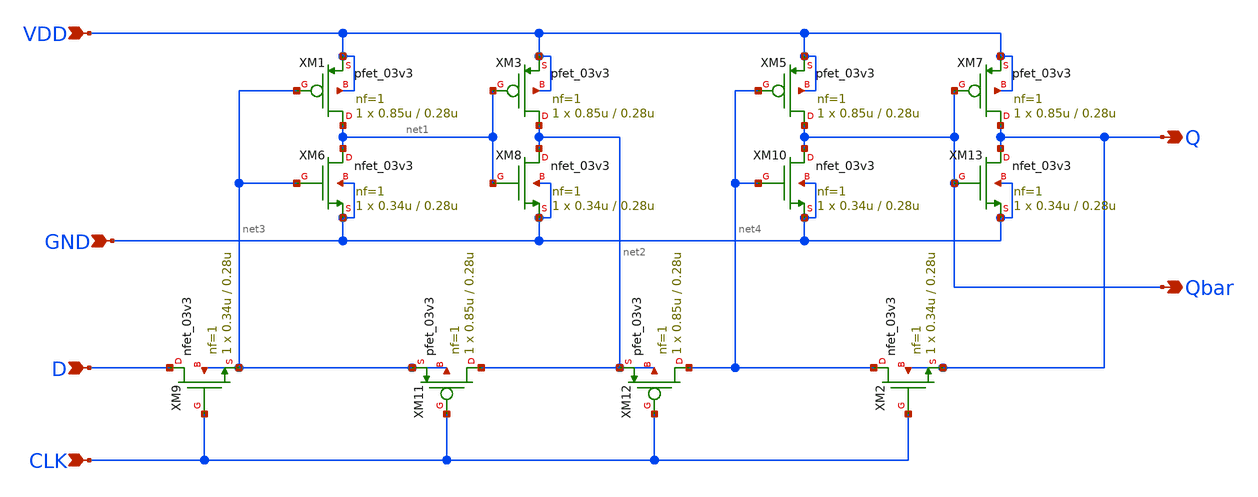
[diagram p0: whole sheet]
** sch_path: Project/1-on-chip/schematic/PNgen/dff.sch
**.subckt dff VDD Q GND D CLK Qbar
*.ipin VDD
*.opin Q
*.ipin GND
*.ipin D
*.ipin CLK
*.opin Qbar
XM9 D CLK net3 net3 nfet_03v3 L=0.28u W=0.34u nf=1 ad='int((nf+1)/2) * W/nf * 0.18u' as='int((nf+2)/2) * W/nf * 0.18u'
+ pd='2*int((nf+1)/2) * (W/nf + 0.18u)' ps='2*int((nf+2)/2) * (W/nf + 0.18u)' nrd='0.18u / W' nrs='0.18u / W'
+ sa=0 sb=0 sd=0 m=1
XM2 net4 CLK Q Q nfet_03v3 L=0.28u W=0.34u nf=1 ad='int((nf+1)/2) * W/nf * 0.18u' as='int((nf+2)/2) * W/nf * 0.18u'
+ pd='2*int((nf+1)/2) * (W/nf + 0.18u)' ps='2*int((nf+2)/2) * (W/nf + 0.18u)' nrd='0.18u / W' nrs='0.18u / W'
+ sa=0 sb=0 sd=0 m=1
XM6 net1 net3 GND GND nfet_03v3 L=0.28u W=0.34u nf=1 ad='int((nf+1)/2) * W/nf * 0.18u' as='int((nf+2)/2) * W/nf * 0.18u'
+ pd='2*int((nf+1)/2) * (W/nf + 0.18u)' ps='2*int((nf+2)/2) * (W/nf + 0.18u)' nrd='0.18u / W' nrs='0.18u / W'
+ sa=0 sb=0 sd=0 m=1
XM8 net2 net1 GND GND nfet_03v3 L=0.28u W=0.34u nf=1 ad='int((nf+1)/2) * W/nf * 0.18u' as='int((nf+2)/2) * W/nf * 0.18u'
+ pd='2*int((nf+1)/2) * (W/nf + 0.18u)' ps='2*int((nf+2)/2) * (W/nf + 0.18u)' nrd='0.18u / W' nrs='0.18u / W'
+ sa=0 sb=0 sd=0 m=1
XM10 Qbar net4 GND GND nfet_03v3 L=0.28u W=0.34u nf=1 ad='int((nf+1)/2) * W/nf * 0.18u' as='int((nf+2)/2) * W/nf * 0.18u'
+ pd='2*int((nf+1)/2) * (W/nf + 0.18u)' ps='2*int((nf+2)/2) * (W/nf + 0.18u)' nrd='0.18u / W' nrs='0.18u / W'
+ sa=0 sb=0 sd=0 m=1
XM13 Q Qbar GND GND nfet_03v3 L=0.28u W=0.34u nf=1 ad='int((nf+1)/2) * W/nf * 0.18u' as='int((nf+2)/2) * W/nf * 0.18u'
+ pd='2*int((nf+1)/2) * (W/nf + 0.18u)' ps='2*int((nf+2)/2) * (W/nf + 0.18u)' nrd='0.18u / W' nrs='0.18u / W'
+ sa=0 sb=0 sd=0 m=1
XM1 net1 net3 VDD VDD pfet_03v3 L=0.28u W=0.85u nf=1 ad='int((nf+1)/2) * W/nf * 0.18u' as='int((nf+2)/2) * W/nf * 0.18u'
+ pd='2*int((nf+1)/2) * (W/nf + 0.18u)' ps='2*int((nf+2)/2) * (W/nf + 0.18u)' nrd='0.18u / W' nrs='0.18u / W'
+ sa=0 sb=0 sd=0 m=1
XM3 net2 net1 VDD VDD pfet_03v3 L=0.28u W=0.85u nf=1 ad='int((nf+1)/2) * W/nf * 0.18u' as='int((nf+2)/2) * W/nf * 0.18u'
+ pd='2*int((nf+1)/2) * (W/nf + 0.18u)' ps='2*int((nf+2)/2) * (W/nf + 0.18u)' nrd='0.18u / W' nrs='0.18u / W'
+ sa=0 sb=0 sd=0 m=1
XM5 Qbar net4 VDD VDD pfet_03v3 L=0.28u W=0.85u nf=1 ad='int((nf+1)/2) * W/nf * 0.18u' as='int((nf+2)/2) * W/nf * 0.18u'
+ pd='2*int((nf+1)/2) * (W/nf + 0.18u)' ps='2*int((nf+2)/2) * (W/nf + 0.18u)' nrd='0.18u / W' nrs='0.18u / W'
+ sa=0 sb=0 sd=0 m=1
XM7 Q Qbar VDD VDD pfet_03v3 L=0.28u W=0.85u nf=1 ad='int((nf+1)/2) * W/nf * 0.18u' as='int((nf+2)/2) * W/nf * 0.18u'
+ pd='2*int((nf+1)/2) * (W/nf + 0.18u)' ps='2*int((nf+2)/2) * (W/nf + 0.18u)' nrd='0.18u / W' nrs='0.18u / W'
+ sa=0 sb=0 sd=0 m=1
XM11 net2 CLK net3 net3 pfet_03v3 L=0.28u W=0.85u nf=1 ad='int((nf+1)/2) * W/nf * 0.18u' as='int((nf+2)/2) * W/nf * 0.18u'
+ pd='2*int((nf+1)/2) * (W/nf + 0.18u)' ps='2*int((nf+2)/2) * (W/nf + 0.18u)' nrd='0.18u / W' nrs='0.18u / W'
+ sa=0 sb=0 sd=0 m=1
XM12 net4 CLK net2 net2 pfet_03v3 L=0.28u W=0.85u nf=1 ad='int((nf+1)/2) * W/nf * 0.18u' as='int((nf+2)/2) * W/nf * 0.18u'
+ pd='2*int((nf+1)/2) * (W/nf + 0.18u)' ps='2*int((nf+2)/2) * (W/nf + 0.18u)' nrd='0.18u / W' nrs='0.18u / W'
+ sa=0 sb=0 sd=0 m=1
**.ends
.end
